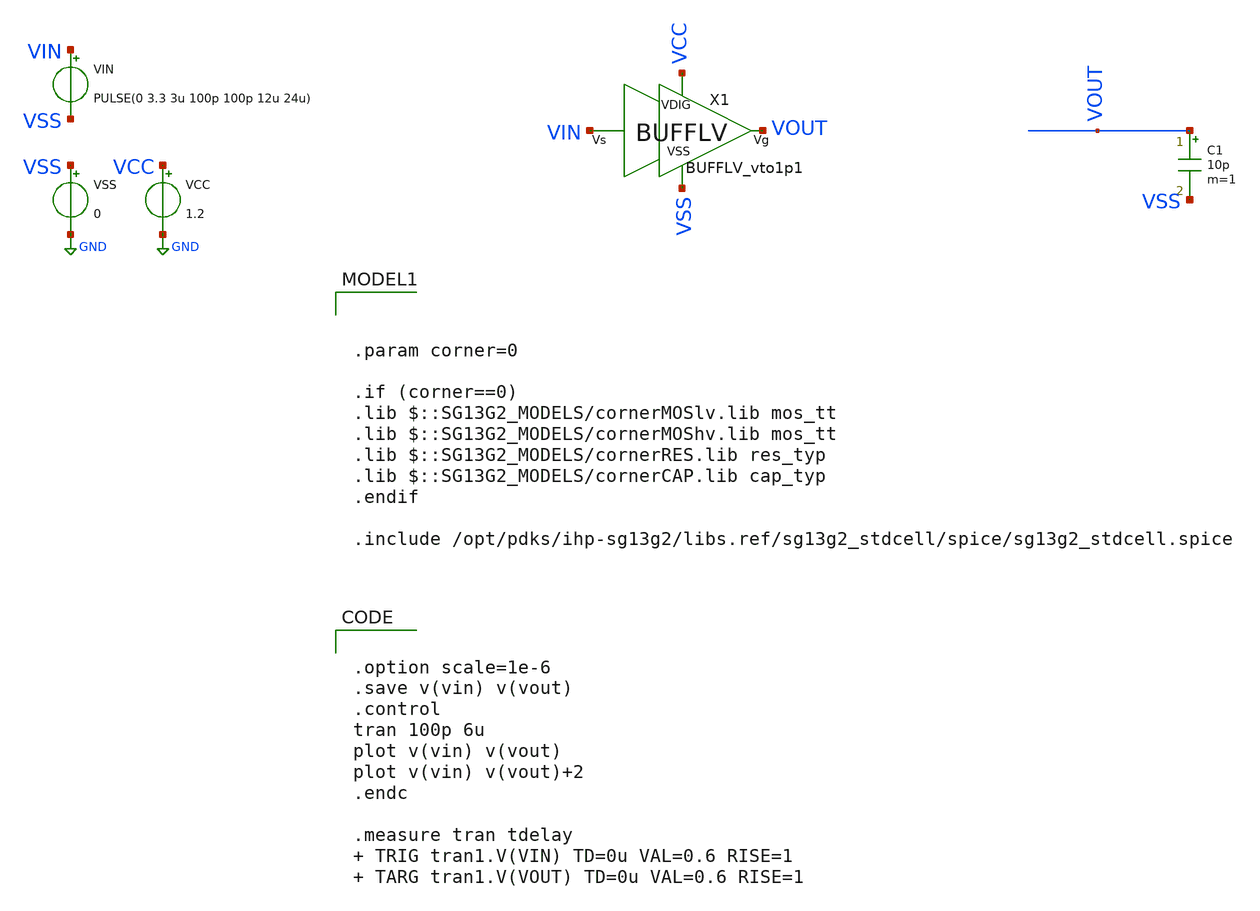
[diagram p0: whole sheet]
** sch_path: AC3E_USM_TDBUCK/design_data/xschem/BUFFLV/tb_BUFFLV_vto1p1.sch
* IHP-GmbH/IHP-Open-PDK/ihp-sg13g2/libs.tech/xschem/sg13g2_stdcells/sg13g2_buf_1.sch:
* Copyright 2023 IHP PDK Authors
* Licensed under the Apache License, Version 2.0 (the "License");
**.subckt tb_BUFFLV_vto1p1
VCC VCC GND 1.2
VSS VSS GND 0
VIN VIN VSS PULSE(0 3.3 3u 100p 100p 12u 24u)
C1 VOUT VSS 10p m=1
X1 VIN VOUT VCC VSS BUFFLV_vto1p1
**** begin user architecture code


.option scale=1e-6
.save v(vin) v(vout)
.control
tran 100p 6u
plot v(vin) v(vout)
plot v(vin) v(vout)+2
.endc

.measure tran tdelay  TRIG tran1.V(VIN) TD=0u VAL=0.6 RISE=1  TARG tran1.V(VOUT) TD=0u VAL=0.6
+ RISE=1






.param corner=0

.if (corner==0)
.lib $::SG13G2_MODELS/cornerMOSlv.lib mos_tt
.lib $::SG13G2_MODELS/cornerMOShv.lib mos_tt
.lib $::SG13G2_MODELS/cornerRES.lib res_typ
.lib $::SG13G2_MODELS/cornerCAP.lib cap_typ
.endif

.include /opt/pdks/ihp-sg13g2/libs.ref/sg13g2_stdcell/spice/sg13g2_stdcell.spice

**** end user architecture code
**.ends

* expanding   symbol:  BUFFLV_vto1p1.sym # of pins=4
** sym_path: AC3E_USM_TDBUCK/design_data/xschem/BUFFLV/BUFFLV_vto1p1.sym
** sch_path: AC3E_USM_TDBUCK/design_data/xschem/BUFFLV/BUFFLV_vto1p1.sch
.subckt BUFFLV_vto1p1 Vs Vg VDIG VSS
*.iopin VDIG
*.ipin Vs
*.opin Vg
*.iopin VSS
x7 net2 net1 VDIG VSS sg13g2_buf_4
x2 net1 Vs VDIG VSS sg13g2_buf_1
x1 net3 net2 VDIG VSS sg13g2_buf_16
x3[0] Vg net3 VDIG VSS sg13g2_buf_16
x3[1] Vg net3 VDIG VSS sg13g2_buf_16
x3[2] Vg net3 VDIG VSS sg13g2_buf_16
x3[3] Vg net3 VDIG VSS sg13g2_buf_16
.ends


* expanding   symbol:  sg13g2_stdcells/sg13g2_buf_4.sym # of pins=2
** sym_path: sg13g2_stdcells/sg13g2_buf_4.sym
** sch_path: sg13g2_stdcells/sg13g2_buf_4.sch
.subckt sg13g2_buf_4 X A VDD VSS
*.ipin A
*.opin X
*.iopin VDD
*.iopin VSS
XM1 net1 A VSS VSS sg13_lv_nmos w=740.00n l=130.00n ng=1 m=1 mm_ok=1
XM2 X net1 VSS VSS sg13_lv_nmos w=2.96u l=130.00n ng=4 m=1 mm_ok=1
XM3 net1 A VDD VDD sg13_lv_pmos w=1.68u l=130.00n ng=2 m=1 mm_ok=1
XM4 X net1 VDD VDD sg13_lv_pmos w=4.48u l=130.00n ng=4 m=1 mm_ok=1
.ends


* expanding   symbol:  sg13g2_stdcells/sg13g2_buf_1.sym # of pins=2
** sym_path: sg13g2_stdcells/sg13g2_buf_1.sym
** sch_path: sg13g2_stdcells/sg13g2_buf_1.sch
.subckt sg13g2_buf_1 X A VDD VSS
*.ipin A
*.opin X
*.iopin VDD
*.iopin VSS
XM1 net1 A VSS VSS sg13_lv_nmos w=550.00n l=130.00n ng=1 m=1 mm_ok=1
XM2 X net1 VSS VSS sg13_lv_nmos w=740.00n l=130.00n ng=1 m=1 mm_ok=1
XM3 net1 A VDD VDD sg13_lv_pmos w=840.00n l=130.00n ng=1 m=1 mm_ok=1
XM4 X net1 VDD VDD sg13_lv_pmos w=1.12u l=130.00n ng=1 m=1 mm_ok=1
.ends


* expanding   symbol:  sg13g2_stdcells/sg13g2_buf_16.sym # of pins=2
** sym_path: sg13g2_stdcells/sg13g2_buf_16.sym
** sch_path: sg13g2_stdcells/sg13g2_buf_16.sch
.subckt sg13g2_buf_16 X A VDD VSS
*.ipin A
*.opin X
*.iopin VDD
*.iopin VSS
XM1 net1 A VSS VSS sg13_lv_nmos w=4.44u l=130.00n ng=6 m=1 mm_ok=1
XM2 X net1 VSS VSS sg13_lv_nmos w=11.84u l=130.00n ng=16 m=1 mm_ok=1
XM3 net1 A VDD VDD sg13_lv_pmos w=6.72u l=130.00n ng=6 m=1 mm_ok=1
XM4 X net1 VDD VDD sg13_lv_pmos w=17.92u l=130.00n ng=16 m=1 mm_ok=1
.ends

.GLOBAL GND
.end
